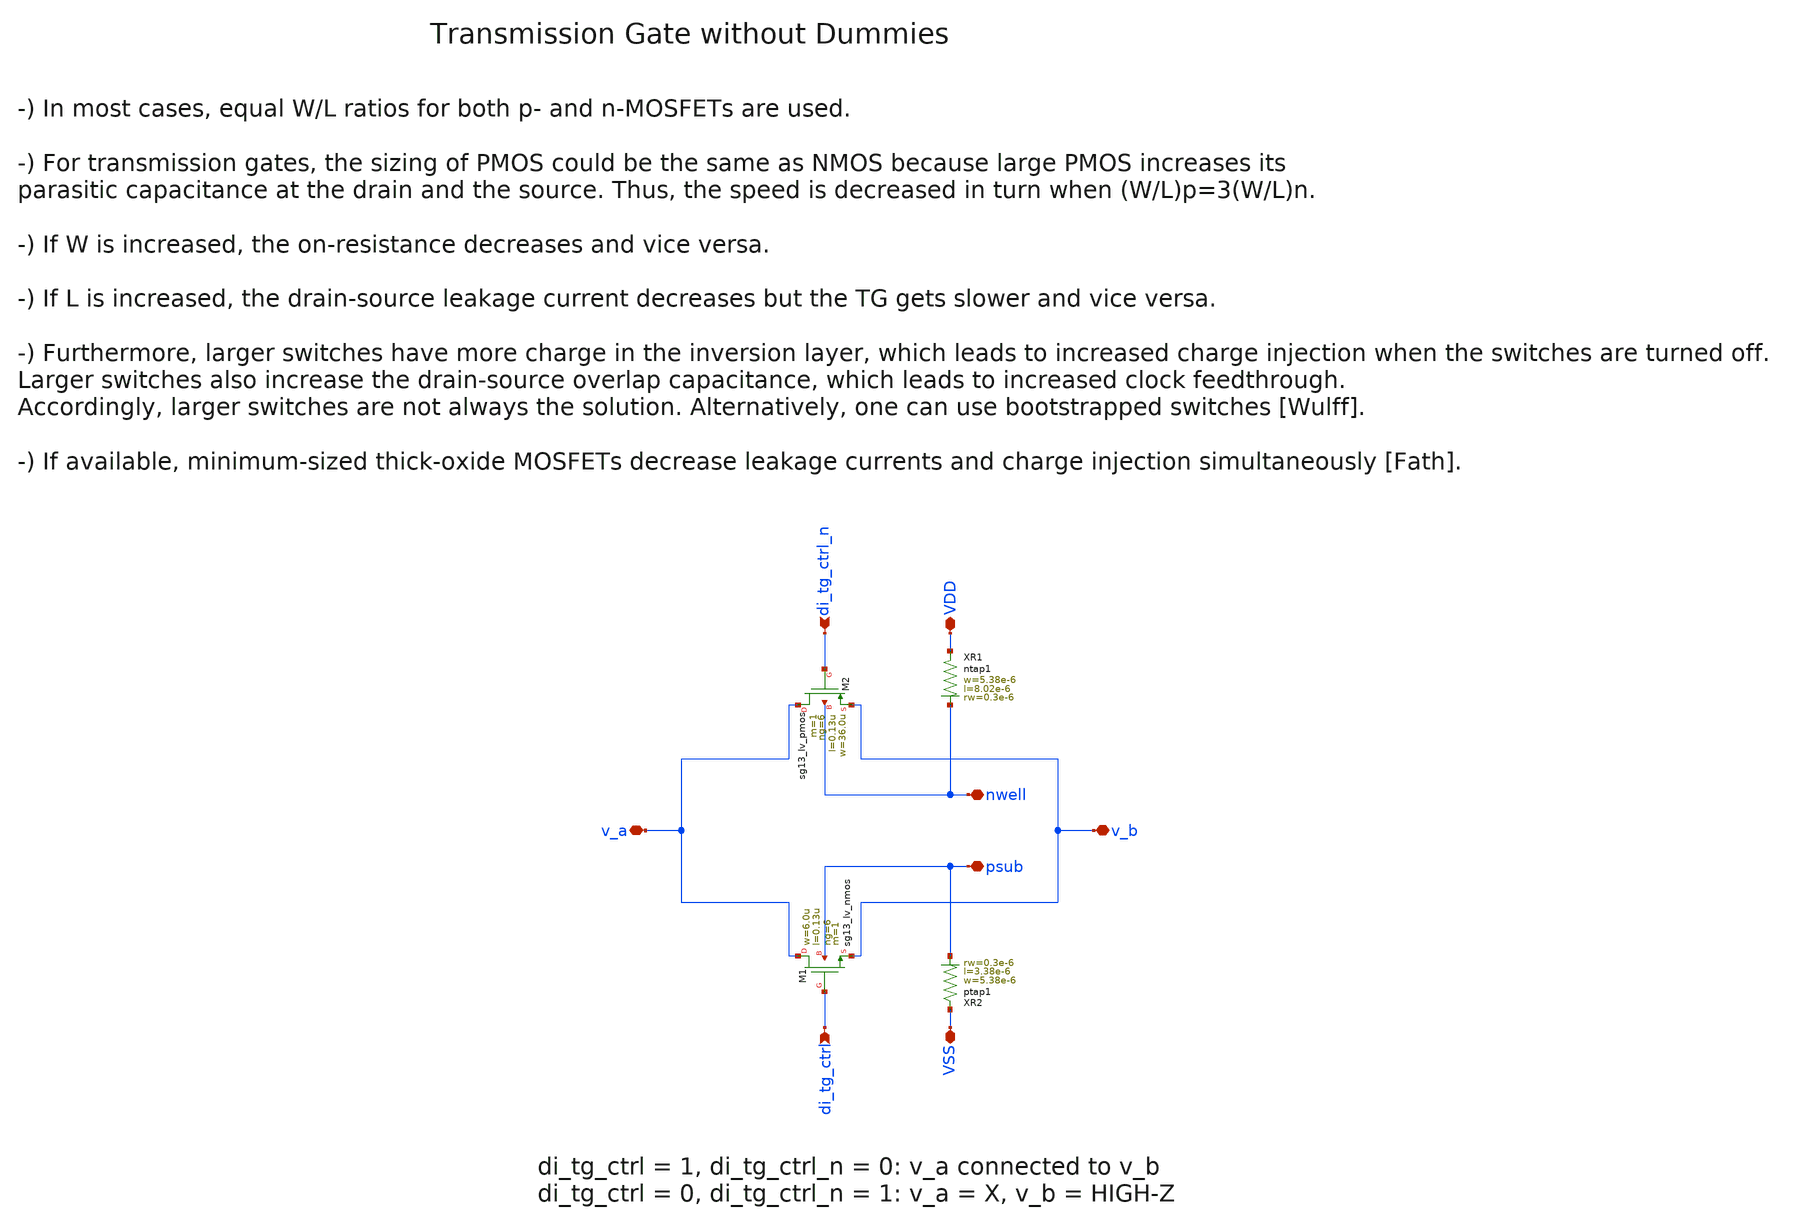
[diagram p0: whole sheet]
** sch_path: ihp130/macros/iqmod/xschem/iqmod_mfb_lpf_ota_core_spdt_switch_tg.sch
**.subckt iqmod_mfb_lpf_ota_core_spdt_switch_tg v_a v_b VDD VSS di_tg_ctrl di_tg_ctrl_n nwell psub
*.iopin v_a
*.iopin v_b
*.iopin VDD
*.iopin VSS
*.ipin di_tg_ctrl
*.ipin di_tg_ctrl_n
*.iopin nwell
*.iopin psub
XM2 v_a di_tg_ctrl_n v_b nwell sg13_lv_pmos w=36.0u l=0.13u ng=6 m=1 mm_ok=1
XM1 v_a di_tg_ctrl v_b psub sg13_lv_nmos w=6.0u l=0.13u ng=6 m=1 mm_ok=1
XR1 VDD nwell ntap1 R=8.903 w=5.38e-6 l=8.02e-6 rw=0.3e-6
XR2 VSS psub ptap1 R=13.96 w=5.38e-6 l=3.38e-6 rw=0.3e-6
**.ends
.end
